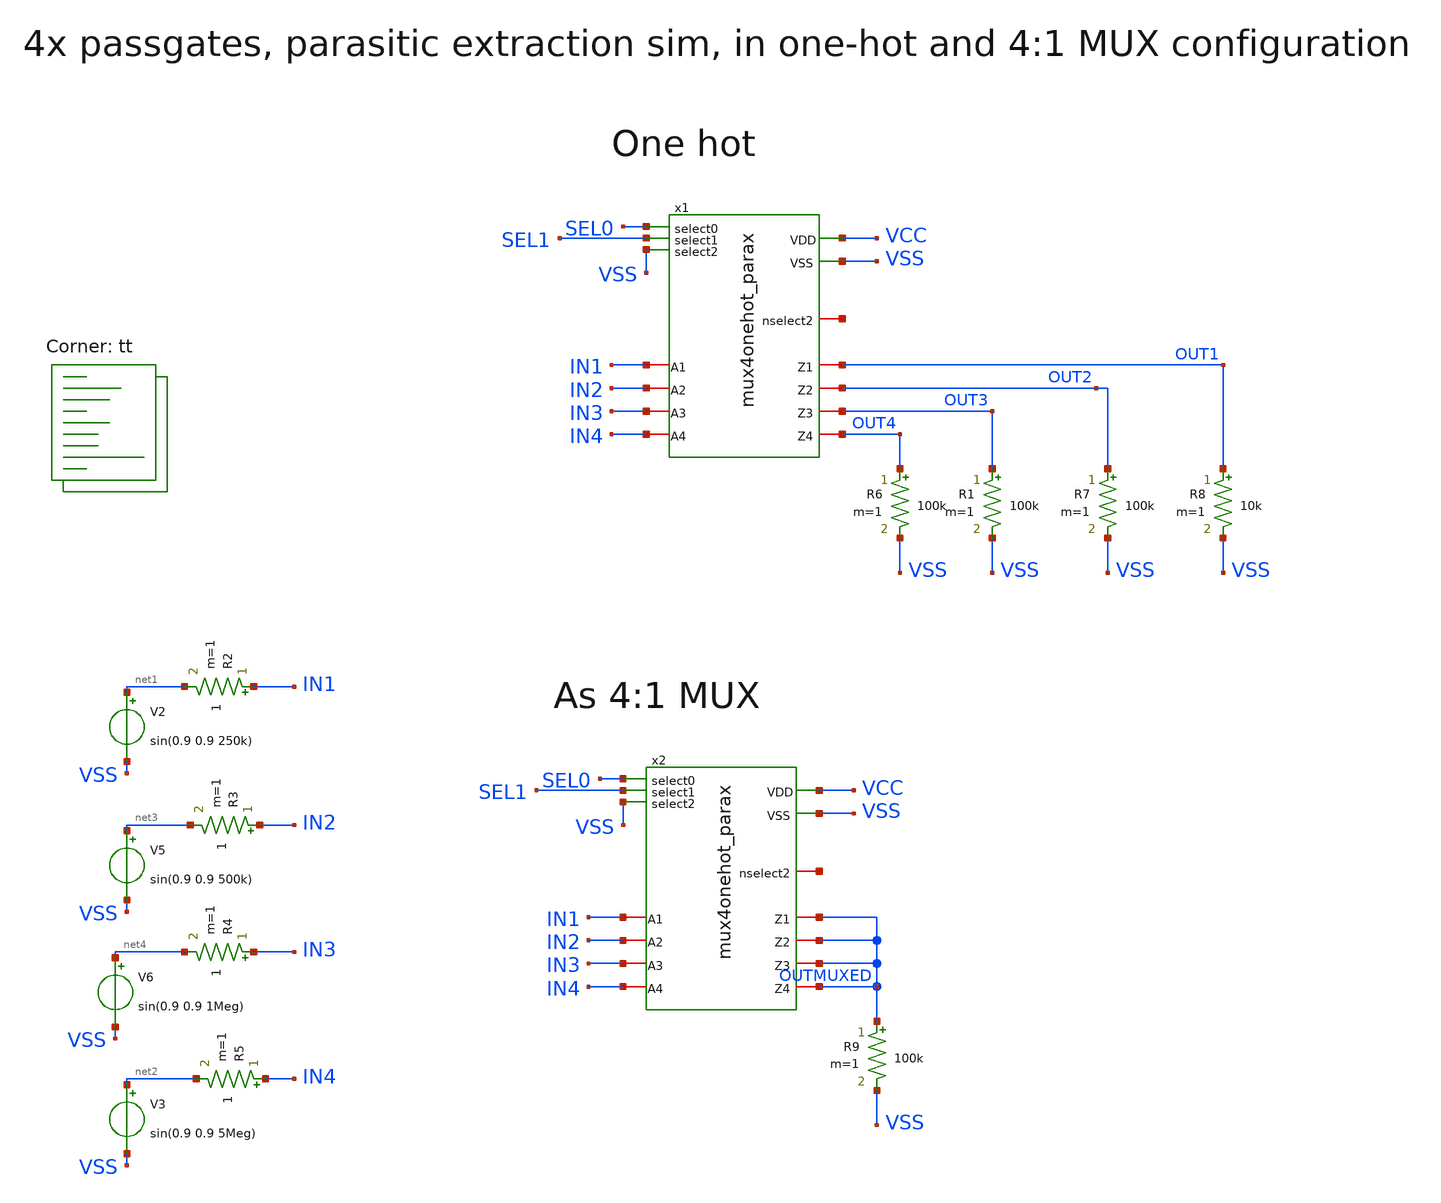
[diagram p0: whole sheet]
** sch_path: xschem/tb_4muxonehot.sch
**.subckt tb_4muxonehot
V2 net1 VSS sin(0.9 0.9 250k)
V3 net2 VSS sin(0.9 0.9 5Meg)
V5 net3 VSS sin(0.9 0.9 500k)
V6 net4 VSS sin(0.9 0.9 1Meg)
R2 IN1 net1 1 m=1
R3 IN2 net3 1 m=1
R4 IN3 net4 1 m=1
R5 IN4 net2 1 m=1
R6 OUT4 VSS 100k m=1
R1 OUT3 VSS 100k m=1
R7 OUT2 VSS 100k m=1
R8 OUT1 VSS 10k m=1
R9 OUTMUXED VSS 100k m=1
x1 SEL0 SEL1 VSS IN1 IN2 IN3 IN4 OUT1 OUT2 OUT3 OUT4 net5 VCC VSS mux4onehot_parax
x2 SEL0 SEL1 VSS IN1 IN2 IN3 IN4 OUTMUXED OUTMUXED OUTMUXED OUTMUXED net6 VCC VSS mux4onehot_parax
**** begin user architecture code
.lib $::SKYWATER_MODELS/sky130.lib.spice tt
**** end user architecture code
**.ends

* expanding   symbol:  mux4onehot_parax.sym # of pins=14
** sym_path: xschem/mux4onehot.sym
.include [file normalize extracted/mux4onehot_parax.spice]
**** begin user architecture code


* ngspice commands
* .options savecurrents
.param VCC = 1.8
.param SRCRES = 1k
.include stimuli_tb_4muxonehot.cir
.control
save all
op
write tb_4muxonehot.raw
set appendwrite
tran 50n 80u
write tb_4muxonehot.raw
* quit 0
.endc



**** end user architecture code
.end
